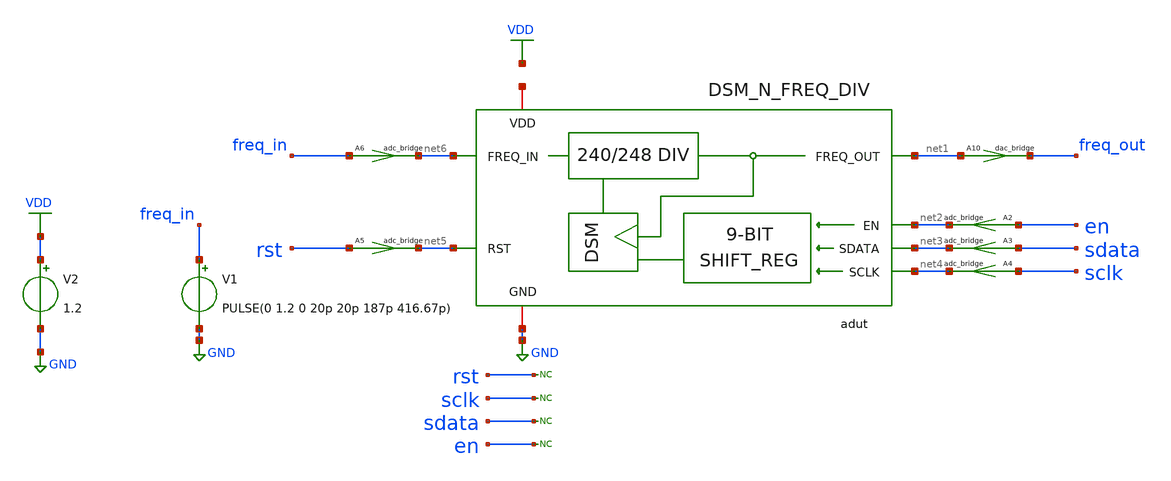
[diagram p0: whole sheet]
** sch_path: xschem/dsm/xschem/tb_DSM_N_FREQ_DIV.sch
* Copyright (C) 1998-2024 Stefan Frederik Schippers
* This program is free software; you can redistribute it and/or modify
* it under the terms of the GNU General Public License as published by
* the Free Software Foundation; either version 2 of the License, or
* (at your option) any later version.
* This program is distributed in the hope that it will be useful,
* but WITHOUT ANY WARRANTY; without even the implied warranty of
* MERCHANTABILITY or FITNESS FOR A PARTICULAR PURPOSE.  See the
* GNU General Public License for more details.
* You should have received a copy of the GNU General Public License
* along with this program; if not, write to the Free Software
**.subckt tb_DSM_N_FREQ_DIV
V1 freq_in GND PULSE(0 1.2 0 20p 20p 187p 416.67p)
A2 [ en ] [ net2 ] adc1
.model adc1 adc_bridge in_low=0.4 in_high=1.2
A3 [ sdata ] [ net3 ] adc1
.model adc1 adc_bridge in_low=0.4 in_high=1.2
A4 [ sclk ] [ net4 ] adc1
.model adc1 adc_bridge in_low=0.4 in_high=1.2
A5 [ rst ] [ net5 ] adc1
.model adc1 adc_bridge in_low=0.4 in_high=1.2
A6 [ freq_in ] [ net6 ] adc1
.model adc1 adc_bridge in_low=0.4 in_high=1.2
* noconn rst
* noconn sclk
* noconn sdata
* noconn en
A10 [ net1 ] [ freq_out ] dac1
.model dac1 dac_bridge out_low=0 out_high=1.2
V2 VDD GND 1.2
adut [ net6 net5 net4 net3 net2 ] [ net1 ] null dut
.model dut d_cosim simulation=../simulations/dsm_and_freq_divider.so
**** begin user architecture code



* ngspice commands
.save v(dout) v(sdata) v(sclk) v(en) v(rst) v(dsm_clk) v(freq_in) v(freq_out)
.control
  tran 10p 250n
  meas tran fo_max max v(freq_out)
  meas tran fo_min min v(freq_out)
  meas tran t_r1 when v(freq_out)=0.6 rise=1
  meas tran t_f1 when v(freq_out)=0.6 fall=1
  meas tran half trig v(freq_out) val=0.6 rise=1 targ v(freq_out) val=0.6 fall=1
  meas tran per trig v(freq_out) val=0.6 rise=1 targ v(freq_out) val=0.6 rise=2
  remzerovec
  write tb_DSM_N_FREQ_DIV.raw
  plot v(freq_out)
.endc

* to generate following file copy stimuli.test
* to the simulation directory and run simulation -> Utile Stimuli Editor (GUI),
* and press 'Translate'
.include stimuli_test.cir



**** end user architecture code
**.ends
.GLOBAL VDD
.GLOBAL GND
.end
